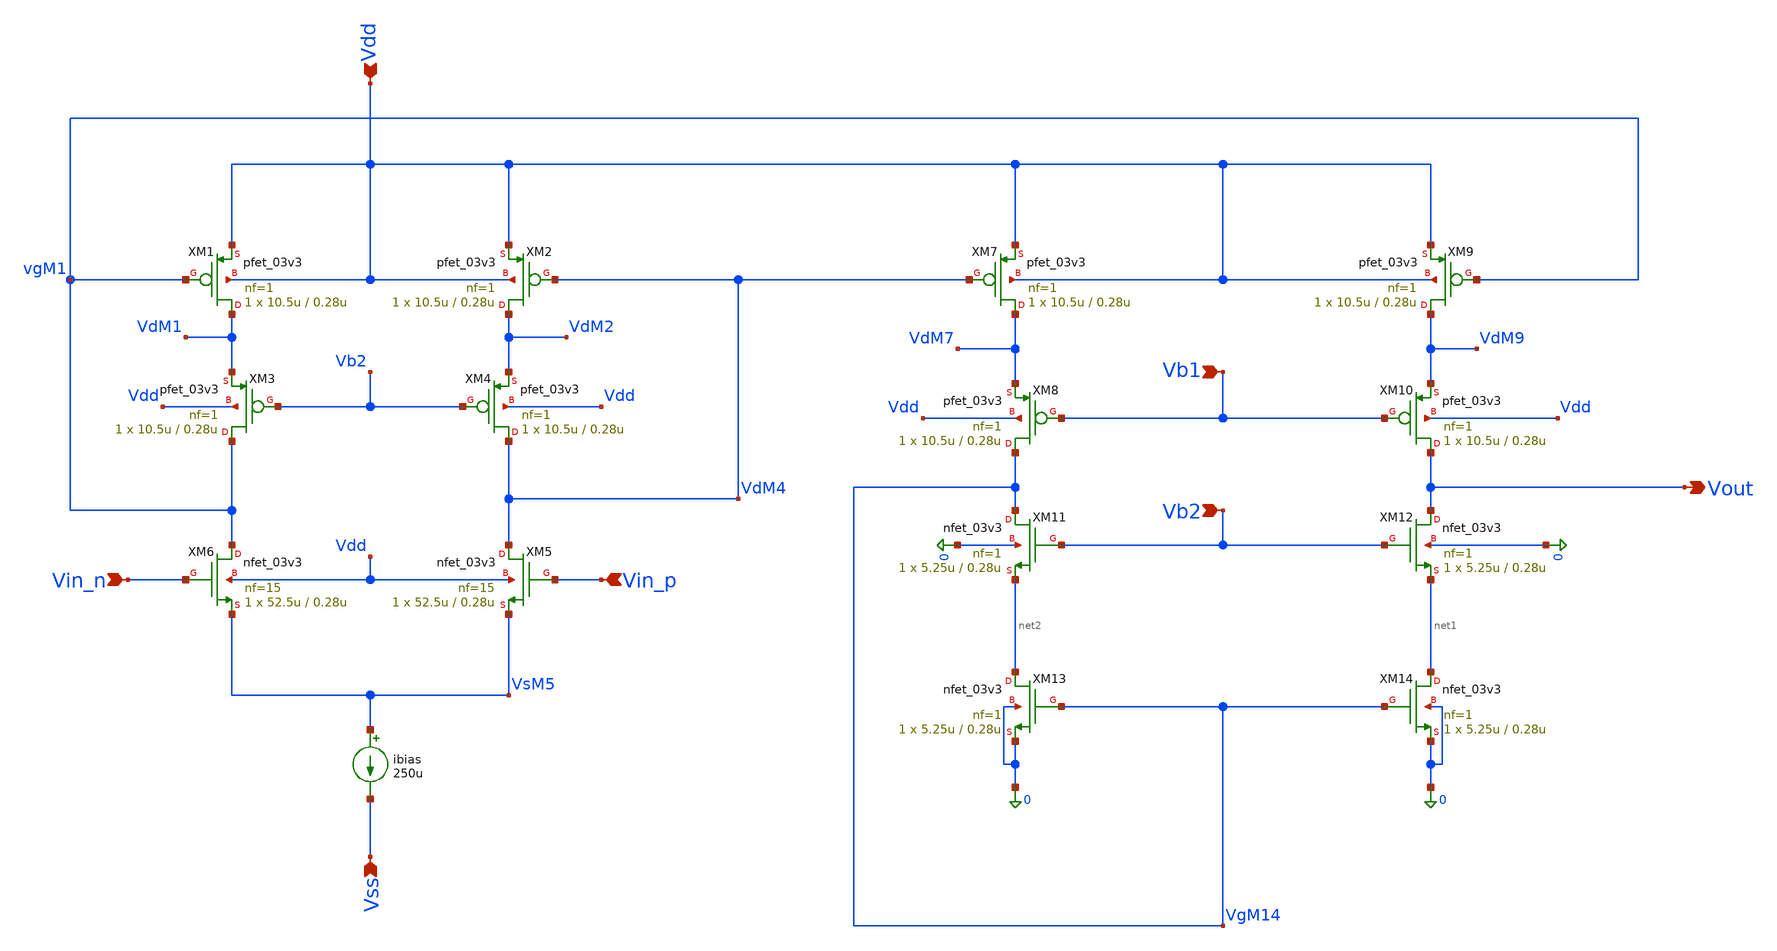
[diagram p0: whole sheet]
** sch_path: blocks/adc/lvds/op_amp.sch
**.subckt op_amp Vdd Vb2 Vin_p Vin_n Vb1 Vout Vss
*.ipin Vdd
*.ipin Vb2
*.ipin Vin_p
*.ipin Vin_n
*.ipin Vb1
*.opin Vout
*.ipin Vss
XM1 VdM1 vgM1 Vdd Vdd pfet_03v3 L=0.28u W=10.5u nf=1 ad='int((nf+1)/2) * W/nf * 0.18u' as='int((nf+2)/2) * W/nf * 0.18u'
+ pd='2*int((nf+1)/2) * (W/nf + 0.18u)' ps='2*int((nf+2)/2) * (W/nf + 0.18u)' nrd='0.18u / W' nrs='0.18u / W'
+ sa=0 sb=0 sd=0 m=1
XM2 VdM2 VdM4 Vdd Vdd pfet_03v3 L=0.28u W=10.5u nf=1 ad='int((nf+1)/2) * W/nf * 0.18u' as='int((nf+2)/2) * W/nf * 0.18u'
+ pd='2*int((nf+1)/2) * (W/nf + 0.18u)' ps='2*int((nf+2)/2) * (W/nf + 0.18u)' nrd='0.18u / W' nrs='0.18u / W'
+ sa=0 sb=0 sd=0 m=1
XM3 vgM1 Vb2 VdM1 Vdd pfet_03v3 L=0.28u W=10.5u nf=1 ad='int((nf+1)/2) * W/nf * 0.18u' as='int((nf+2)/2) * W/nf * 0.18u'
+ pd='2*int((nf+1)/2) * (W/nf + 0.18u)' ps='2*int((nf+2)/2) * (W/nf + 0.18u)' nrd='0.18u / W' nrs='0.18u / W'
+ sa=0 sb=0 sd=0 m=1
XM4 VdM4 Vb2 VdM2 Vdd pfet_03v3 L=0.28u W=10.5u nf=1 ad='int((nf+1)/2) * W/nf * 0.18u' as='int((nf+2)/2) * W/nf * 0.18u'
+ pd='2*int((nf+1)/2) * (W/nf + 0.18u)' ps='2*int((nf+2)/2) * (W/nf + 0.18u)' nrd='0.18u / W' nrs='0.18u / W'
+ sa=0 sb=0 sd=0 m=1
XM5 VdM4 Vin_p VsM5 Vdd nfet_03v3 L=0.28u W=52.5u nf=15 ad='int((nf+1)/2) * W/nf * 0.18u' as='int((nf+2)/2) * W/nf * 0.18u'
+ pd='2*int((nf+1)/2) * (W/nf + 0.18u)' ps='2*int((nf+2)/2) * (W/nf + 0.18u)' nrd='0.18u / W' nrs='0.18u / W'
+ sa=0 sb=0 sd=0 m=1
XM6 vgM1 Vin_n VsM5 Vdd nfet_03v3 L=0.28u W=52.5u nf=15 ad='int((nf+1)/2) * W/nf * 0.18u' as='int((nf+2)/2) * W/nf * 0.18u'
+ pd='2*int((nf+1)/2) * (W/nf + 0.18u)' ps='2*int((nf+2)/2) * (W/nf + 0.18u)' nrd='0.18u / W' nrs='0.18u / W'
+ sa=0 sb=0 sd=0 m=1
XM7 VdM7 VdM4 Vdd Vdd pfet_03v3 L=0.28u W=10.5u nf=1 ad='int((nf+1)/2) * W/nf * 0.18u' as='int((nf+2)/2) * W/nf * 0.18u'
+ pd='2*int((nf+1)/2) * (W/nf + 0.18u)' ps='2*int((nf+2)/2) * (W/nf + 0.18u)' nrd='0.18u / W' nrs='0.18u / W'
+ sa=0 sb=0 sd=0 m=1
XM9 VdM9 vgM1 Vdd Vdd pfet_03v3 L=0.28u W=10.5u nf=1 ad='int((nf+1)/2) * W/nf * 0.18u' as='int((nf+2)/2) * W/nf * 0.18u'
+ pd='2*int((nf+1)/2) * (W/nf + 0.18u)' ps='2*int((nf+2)/2) * (W/nf + 0.18u)' nrd='0.18u / W' nrs='0.18u / W'
+ sa=0 sb=0 sd=0 m=1
XM11 VgM14 Vb2 net2 0 nfet_03v3 L=0.28u W=5.25u nf=1 ad='int((nf+1)/2) * W/nf * 0.18u' as='int((nf+2)/2) * W/nf * 0.18u'
+ pd='2*int((nf+1)/2) * (W/nf + 0.18u)' ps='2*int((nf+2)/2) * (W/nf + 0.18u)' nrd='0.18u / W' nrs='0.18u / W'
+ sa=0 sb=0 sd=0 m=1
XM12 Vout Vb2 net1 0 nfet_03v3 L=0.28u W=5.25u nf=1 ad='int((nf+1)/2) * W/nf * 0.18u' as='int((nf+2)/2) * W/nf * 0.18u'
+ pd='2*int((nf+1)/2) * (W/nf + 0.18u)' ps='2*int((nf+2)/2) * (W/nf + 0.18u)' nrd='0.18u / W' nrs='0.18u / W'
+ sa=0 sb=0 sd=0 m=1
XM13 net2 VgM14 0 0 nfet_03v3 L=0.28u W=5.25u nf=1 ad='int((nf+1)/2) * W/nf * 0.18u' as='int((nf+2)/2) * W/nf * 0.18u'
+ pd='2*int((nf+1)/2) * (W/nf + 0.18u)' ps='2*int((nf+2)/2) * (W/nf + 0.18u)' nrd='0.18u / W' nrs='0.18u / W'
+ sa=0 sb=0 sd=0 m=1
XM14 net1 VgM14 0 0 nfet_03v3 L=0.28u W=5.25u nf=1 ad='int((nf+1)/2) * W/nf * 0.18u' as='int((nf+2)/2) * W/nf * 0.18u'
+ pd='2*int((nf+1)/2) * (W/nf + 0.18u)' ps='2*int((nf+2)/2) * (W/nf + 0.18u)' nrd='0.18u / W' nrs='0.18u / W'
+ sa=0 sb=0 sd=0 m=1
ibias VsM5 Vss 250u
XM8 VgM14 Vb1 VdM7 Vdd pfet_03v3 L=0.28u W=10.5u nf=1 ad='int((nf+1)/2) * W/nf * 0.18u' as='int((nf+2)/2) * W/nf * 0.18u'
+ pd='2*int((nf+1)/2) * (W/nf + 0.18u)' ps='2*int((nf+2)/2) * (W/nf + 0.18u)' nrd='0.18u / W' nrs='0.18u / W'
+ sa=0 sb=0 sd=0 m=1
XM10 Vout Vb1 VdM9 Vdd pfet_03v3 L=0.28u W=10.5u nf=1 ad='int((nf+1)/2) * W/nf * 0.18u' as='int((nf+2)/2) * W/nf * 0.18u'
+ pd='2*int((nf+1)/2) * (W/nf + 0.18u)' ps='2*int((nf+2)/2) * (W/nf + 0.18u)' nrd='0.18u / W' nrs='0.18u / W'
+ sa=0 sb=0 sd=0 m=1
**.ends
.end
